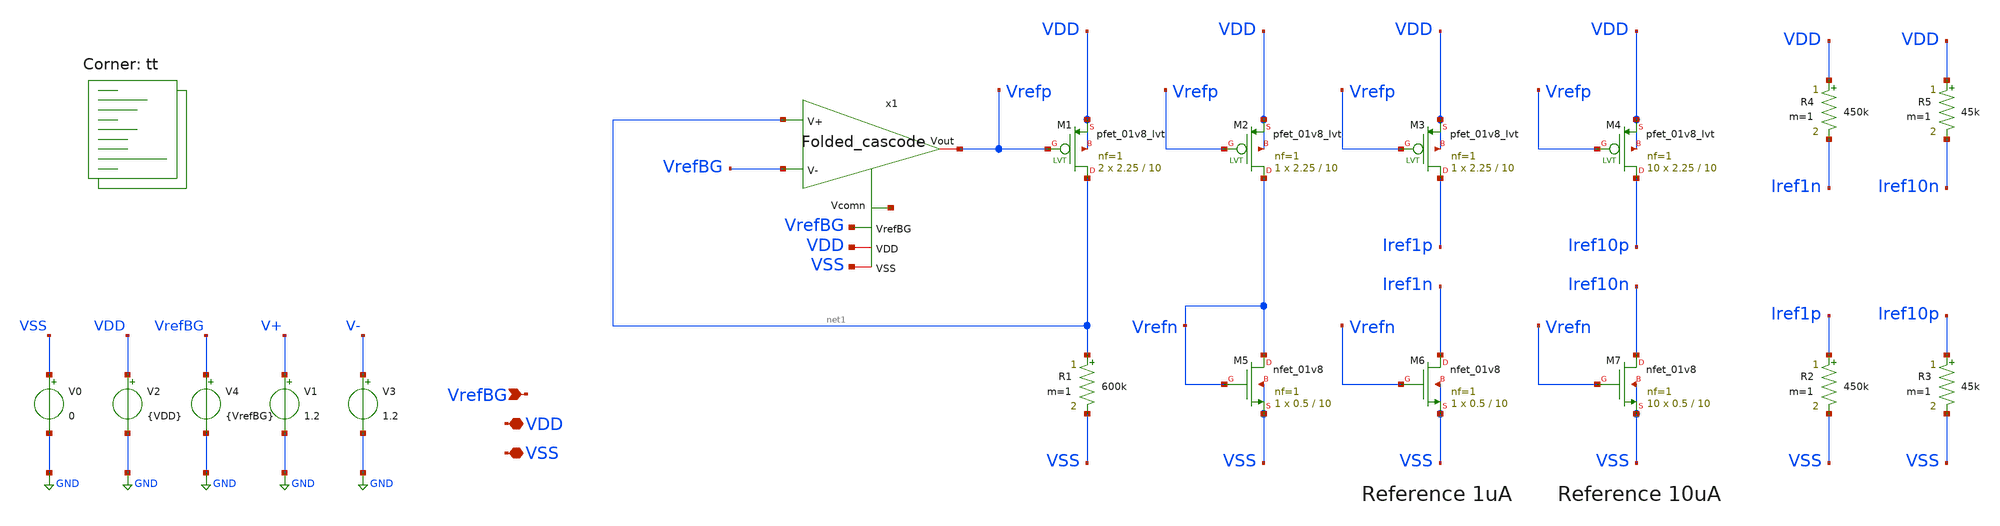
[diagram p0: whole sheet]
** sch_path: openfasoc/generators/curref-gen/sch/Current_reference_generator.sch
**.subckt Current_reference_generator VrefBG VDD VSS
*.ipin VrefBG
*.iopin VDD
*.iopin VSS
x1 Vrefp net1 VrefBG VrefBG VDD VSS net2 Folded_cascode
XM1 net1 Vrefp VDD VDD sky130_fd_pr__pfet_01v8_lvt L=10 W=2.25 nf=1 ad='int((1 + 1)/2) * 2.25 / 1 * 0.29'
+ as='int((1 + 2)/2) * 2.25 / 1 * 0.29' pd='2*int((1 + 1)/2) * (2.25 / 1 + 0.29)' ps='2*int((1 + 2)/2) * (2.25 / 1 + 0.29)'
+ nrd='0.29 / 2.25 ' nrs='0.29 / 2.25 ' sa=0 sb=0 sd=0 mult=2 m=2
R1 net1 VSS 600k m=1
XM2 Vrefn Vrefp VDD VDD sky130_fd_pr__pfet_01v8_lvt L=10 W=2.25 nf=1 ad='int((1 + 1)/2) * 2.25 / 1 * 0.29'
+ as='int((1 + 2)/2) * 2.25 / 1 * 0.29' pd='2*int((1 + 1)/2) * (2.25 / 1 + 0.29)' ps='2*int((1 + 2)/2) * (2.25 / 1 + 0.29)'
+ nrd='0.29 / 2.25 ' nrs='0.29 / 2.25 ' sa=0 sb=0 sd=0 mult=1 m=1
XM5 Vrefn Vrefn VSS VSS sky130_fd_pr__nfet_01v8 L=10 W=0.5 nf=1 ad='int((nf+1)/2) * W/nf * 0.29' as='int((nf+2)/2) * W/nf * 0.29'
+ pd='2*int((nf+1)/2) * (W/nf + 0.29)' ps='2*int((nf+2)/2) * (W/nf + 0.29)' nrd='0.29 / W' nrs='0.29 / W'
+ sa=0 sb=0 sd=0 mult=1 m=1
XM6 Iref1n Vrefn VSS VSS sky130_fd_pr__nfet_01v8 L=10 W=0.5 nf=1 ad='int((nf+1)/2) * W/nf * 0.29' as='int((nf+2)/2) * W/nf * 0.29'
+ pd='2*int((nf+1)/2) * (W/nf + 0.29)' ps='2*int((nf+2)/2) * (W/nf + 0.29)' nrd='0.29 / W' nrs='0.29 / W'
+ sa=0 sb=0 sd=0 mult=1 m=1
XM3 Iref1p Vrefp VDD VDD sky130_fd_pr__pfet_01v8_lvt L=10 W=2.25 nf=1 ad='int((1 + 1)/2) * 2.25 / 1 * 0.29'
+ as='int((1 + 2)/2) * 2.25 / 1 * 0.29' pd='2*int((1 + 1)/2) * (2.25 / 1 + 0.29)' ps='2*int((1 + 2)/2) * (2.25 / 1 + 0.29)'
+ nrd='0.29 / 2.25 ' nrs='0.29 / 2.25 ' sa=0 sb=0 sd=0 mult=1 m=1
XM7 Iref10n Vrefn VSS VSS sky130_fd_pr__nfet_01v8 L=10 W=0.5 nf=1 ad='int((nf+1)/2) * W/nf * 0.29' as='int((nf+2)/2) * W/nf * 0.29'
+ pd='2*int((nf+1)/2) * (W/nf + 0.29)' ps='2*int((nf+2)/2) * (W/nf + 0.29)' nrd='0.29 / W' nrs='0.29 / W'
+ sa=0 sb=0 sd=0 mult=10 m=10
XM4 Iref10p Vrefp VDD VDD sky130_fd_pr__pfet_01v8_lvt L=10 W=2.25 nf=1 ad='int((1 + 1)/2) * 2.25 / 1 * 0.29'
+ as='int((1 + 2)/2) * 2.25 / 1 * 0.29' pd='2*int((1 + 1)/2) * (2.25 / 1 + 0.29)' ps='2*int((1 + 2)/2) * (2.25 / 1 + 0.29)'
+ nrd='0.29 / 2.25 ' nrs='0.29 / 2.25 ' sa=0 sb=0 sd=0 mult=10 m=10
V0 VSS GND 0
V2 VDD GND {VDD}
V4 VrefBG GND {VrefBG}
V1 V+ GND 1.2
V3 V- GND 1.2
R2 Iref1p VSS 450k m=1
R3 Iref10p VSS 45k m=1
R4 VDD Iref1n 450k m=1
R5 VDD Iref10n 45k m=1
**** begin user architecture code
.lib $::SKYWATER_MODELS/sky130.lib.spice tt



.param VDD=1.8
.param VrefBG=1.2
.save

*nfet
  @m.xm5.msky130_fd_pr__nfet_01v8[gm]  v(@m.xm5.msky130_fd_pr__nfet_01v8[vth])
+  @m.xm5.msky130_fd_pr__nfet_01v8[gds]  @m.xm5.msky130_fd_pr__nfet_01v8[id]
  @m.xm6.msky130_fd_pr__nfet_01v8[gm]  v(@m.xm6.msky130_fd_pr__nfet_01v8[vth])
+  @m.xm6.msky130_fd_pr__nfet_01v8[gds]  @m.xm6.msky130_fd_pr__nfet_01v8[id]
  @m.xm7.msky130_fd_pr__nfet_01v8[gm]  v(@m.xm7.msky130_fd_pr__nfet_01v8[vth])
+  @m.xm7.msky130_fd_pr__nfet_01v8[gds]  @m.xm7.msky130_fd_pr__nfet_01v8[id]

*pfet
  @m.xm1.msky130_fd_pr__pfet_01v8_lvt[gm]  v(@m.xm1.msky130_fd_pr__pfet_01v8_lvt[vth])
+  @m.xm1.msky130_fd_pr__pfet_01v8_lvt[gds]  @m.xm1.msky130_fd_pr__pfet_01v8_lvt[id]
  @m.xm2.msky130_fd_pr__pfet_01v8_lvt[gm]  v(@m.xm2.msky130_fd_pr__pfet_01v8_lvt[vth])
+  @m.xm2.msky130_fd_pr__pfet_01v8_lvt[gds]  @m.xm2.msky130_fd_pr__pfet_01v8_lvt[id]
  @m.xm3.msky130_fd_pr__pfet_01v8_lvt[gm]  v(@m.xm3.msky130_fd_pr__pfet_01v8_lvt[vth])
+  @m.xm3.msky130_fd_pr__pfet_01v8_lvt[gds]  @m.xm3.msky130_fd_pr__pfet_01v8_lvt[id]
  @m.xm4.msky130_fd_pr__pfet_01v8_lvt[gm]  v(@m.xm4.msky130_fd_pr__pfet_01v8_lvt[vth])
+  @m.xm4.msky130_fd_pr__pfet_01v8_lvt[gds]  @m.xm4.msky130_fd_pr__pfet_01v8_lvt[id]

.control
  save all
  op
  show
  write Current_reference_generator.raw
.endc



**** end user architecture code
**.ends

* expanding   symbol:  /foss/designs/Folded_cascode/Folded_cascode.sym # of pins=7
** sym_path: openfasoc/generators/curref-gen/sch/Folded_cascode.sym
** sch_path: openfasoc/generators/curref-gen/sch/Folded_cascode.sch
.subckt Folded_cascode Vout V+ V- VrefBG VDD VSS Vcomn
*.ipin V+
*.ipin V-
*.ipin VrefBG
*.iopin VDD
*.iopin VSS
*.iopin Vout
*.iopin Vcomn
XM6 net2 V- net5 net5 sky130_fd_pr__nfet_01v8 L=1 W=1 nf=1 ad='int((nf+1)/2) * W/nf * 0.29' as='int((nf+2)/2) * W/nf * 0.29'
+ pd='2*int((nf+1)/2) * (W/nf + 0.29)' ps='2*int((nf+2)/2) * (W/nf + 0.29)' nrd='0.29 / W' nrs='0.29 / W'
+ sa=0 sb=0 sd=0 mult=20 m=20
XM7 Vout VB2 Vcomn VSS sky130_fd_pr__nfet_01v8 L=3 W=1 nf=1 ad='int((nf+1)/2) * W/nf * 0.29' as='int((nf+2)/2) * W/nf * 0.29'
+ pd='2*int((nf+1)/2) * (W/nf + 0.29)' ps='2*int((nf+2)/2) * (W/nf + 0.29)' nrd='0.29 / W' nrs='0.29 / W'
+ sa=0 sb=0 sd=0 mult=5 m=5
XM8 net4 VB2 net3 VSS sky130_fd_pr__nfet_01v8 L=3 W=1 nf=1 ad='int((nf+1)/2) * W/nf * 0.29' as='int((nf+2)/2) * W/nf * 0.29'
+ pd='2*int((nf+1)/2) * (W/nf + 0.29)' ps='2*int((nf+2)/2) * (W/nf + 0.29)' nrd='0.29 / W' nrs='0.29 / W'
+ sa=0 sb=0 sd=0 mult=5 m=5
XM9 Vcomn VP VSS VSS sky130_fd_pr__nfet_01v8 L=6.5 W=0.5 nf=1 ad='int((nf+1)/2) * W/nf * 0.29' as='int((nf+2)/2) * W/nf * 0.29'
+ pd='2*int((nf+1)/2) * (W/nf + 0.29)' ps='2*int((nf+2)/2) * (W/nf + 0.29)' nrd='0.29 / W' nrs='0.29 / W'
+ sa=0 sb=0 sd=0 mult=5 m=5
XM10 net3 VP VSS VSS sky130_fd_pr__nfet_01v8 L=6.5 W=0.5 nf=1 ad='int((nf+1)/2) * W/nf * 0.29' as='int((nf+2)/2) * W/nf * 0.29'
+ pd='2*int((nf+1)/2) * (W/nf + 0.29)' ps='2*int((nf+2)/2) * (W/nf + 0.29)' nrd='0.29 / W' nrs='0.29 / W'
+ sa=0 sb=0 sd=0 mult=5 m=5
XM11 net5 VP VSS VSS sky130_fd_pr__nfet_01v8 L=6.5 W=0.5 nf=1 ad='int((nf+1)/2) * W/nf * 0.29' as='int((nf+2)/2) * W/nf * 0.29'
+ pd='2*int((nf+1)/2) * (W/nf + 0.29)' ps='2*int((nf+2)/2) * (W/nf + 0.29)' nrd='0.29 / W' nrs='0.29 / W'
+ sa=0 sb=0 sd=0 mult=10 m=10
XM1 net1 V+ net5 net5 sky130_fd_pr__nfet_01v8 L=1 W=1 nf=1 ad='int((nf+1)/2) * W/nf * 0.29' as='int((nf+2)/2) * W/nf * 0.29'
+ pd='2*int((nf+1)/2) * (W/nf + 0.29)' ps='2*int((nf+2)/2) * (W/nf + 0.29)' nrd='0.29 / W' nrs='0.29 / W'
+ sa=0 sb=0 sd=0 mult=20 m=20
XM12 VP VP VSS VSS sky130_fd_pr__nfet_01v8 L=6.5 W=0.5 nf=1 ad='int((nf+1)/2) * W/nf * 0.29' as='int((nf+2)/2) * W/nf * 0.29'
+ pd='2*int((nf+1)/2) * (W/nf + 0.29)' ps='2*int((nf+2)/2) * (W/nf + 0.29)' nrd='0.29 / W' nrs='0.29 / W'
+ sa=0 sb=0 sd=0 mult=1 m=1
XM13 net6 VP VSS VSS sky130_fd_pr__nfet_01v8 L=6.5 W=0.5 nf=1 ad='int((nf+1)/2) * W/nf * 0.29' as='int((nf+2)/2) * W/nf * 0.29'
+ pd='2*int((nf+1)/2) * (W/nf + 0.29)' ps='2*int((nf+2)/2) * (W/nf + 0.29)' nrd='0.29 / W' nrs='0.29 / W'
+ sa=0 sb=0 sd=0 mult=1 m=1
XM17 VB2 VB2 VSS VSS sky130_fd_pr__nfet_01v8 L=18 W=0.42 nf=1 ad='int((nf+1)/2) * W/nf * 0.29' as='int((nf+2)/2) * W/nf * 0.29'
+ pd='2*int((nf+1)/2) * (W/nf + 0.29)' ps='2*int((nf+2)/2) * (W/nf + 0.29)' nrd='0.29 / W' nrs='0.29 / W'
+ sa=0 sb=0 sd=0 mult=1 m=1
XM18 VB2 net6 VDD VDD sky130_fd_pr__pfet_01v8_lvt L=6 W=0.5 nf=1 ad='int((1 + 1)/2) * 0.5 / 1 * 0.29'
+ as='int((1 + 2)/2) * 0.5 / 1 * 0.29' pd='2*int((1 + 1)/2) * (0.5 / 1 + 0.29)' ps='2*int((1 + 2)/2) * (0.5 / 1 + 0.29)'
+ nrd='0.29 / 0.5 ' nrs='0.29 / 0.5 ' sa=0 sb=0 sd=0 mult=4 m=4
XM15 net6 net6 VDD VDD sky130_fd_pr__pfet_01v8_lvt L=6 W=0.5 nf=1 ad='int((1 + 1)/2) * 0.5 / 1 * 0.29'
+ as='int((1 + 2)/2) * 0.5 / 1 * 0.29' pd='2*int((1 + 1)/2) * (0.5 / 1 + 0.29)' ps='2*int((1 + 2)/2) * (0.5 / 1 + 0.29)'
+ nrd='0.29 / 0.5 ' nrs='0.29 / 0.5 ' sa=0 sb=0 sd=0 mult=4 m=4
XM3 net1 net4 VDD VDD sky130_fd_pr__pfet_01v8_lvt L=3 W=1 nf=1 ad='int((1 + 1)/2) * 1 / 1 * 0.29' as='int((1 + 2)/2) * 1 / 1 * 0.29'
+ pd='2*int((1 + 1)/2) * (1 / 1 + 0.29)' ps='2*int((1 + 2)/2) * (1 / 1 + 0.29)' nrd='0.29 / 1 ' nrs='0.29 / 1 '
+ sa=0 sb=0 sd=0 mult=6 m=6
XM2 net2 net4 VDD VDD sky130_fd_pr__pfet_01v8_lvt L=3 W=1 nf=1 ad='int((1 + 1)/2) * 1 / 1 * 0.29' as='int((1 + 2)/2) * 1 / 1 * 0.29'
+ pd='2*int((1 + 1)/2) * (1 / 1 + 0.29)' ps='2*int((1 + 2)/2) * (1 / 1 + 0.29)' nrd='0.29 / 1 ' nrs='0.29 / 1 '
+ sa=0 sb=0 sd=0 mult=6 m=6
XM5 net4 VB1 net1 VDD sky130_fd_pr__pfet_01v8_lvt L=1.5 W=1 nf=1 ad='int((1 + 1)/2) * 1 / 1 * 0.29' as='int((1 + 2)/2) * 1 / 1 * 0.29'
+ pd='2*int((1 + 1)/2) * (1 / 1 + 0.29)' ps='2*int((1 + 2)/2) * (1 / 1 + 0.29)' nrd='0.29 / 1 ' nrs='0.29 / 1 '
+ sa=0 sb=0 sd=0 mult=10 m=10
XM16 Vout VB1 net2 VDD sky130_fd_pr__pfet_01v8_lvt L=1.5 W=1 nf=1 ad='int((1 + 1)/2) * 1 / 1 * 0.29'
+ as='int((1 + 2)/2) * 1 / 1 * 0.29' pd='2*int((1 + 1)/2) * (1 / 1 + 0.29)' ps='2*int((1 + 2)/2) * (1 / 1 + 0.29)'
+ nrd='0.29 / 1 ' nrs='0.29 / 1 ' sa=0 sb=0 sd=0 mult=10 m=10
XM4 VP VB1 VDD VDD sky130_fd_pr__pfet_01v8_lvt L=6 W=0.5 nf=1 ad='int((1 + 1)/2) * 0.5 / 1 * 0.29' as='int((1 + 2)/2) * 0.5 / 1 * 0.29'
+ pd='2*int((1 + 1)/2) * (0.5 / 1 + 0.29)' ps='2*int((1 + 2)/2) * (0.5 / 1 + 0.29)' nrd='0.29 / 0.5 ' nrs='0.29 / 0.5 '
+ sa=0 sb=0 sd=0 mult=1 m=1
XM14 VB1 VB1 VDD VDD sky130_fd_pr__pfet_01v8_lvt L=6 W=0.5 nf=1 ad='int((1 + 1)/2) * 0.5 / 1 * 0.29'
+ as='int((1 + 2)/2) * 0.5 / 1 * 0.29' pd='2*int((1 + 1)/2) * (0.5 / 1 + 0.29)' ps='2*int((1 + 2)/2) * (0.5 / 1 + 0.29)'
+ nrd='0.29 / 0.5 ' nrs='0.29 / 0.5 ' sa=0 sb=0 sd=0 mult=1 m=1
XM19 VB1 VrefBG VSS VSS sky130_fd_pr__nfet_01v8 L=18 W=0.45 nf=1 ad='int((nf+1)/2) * W/nf * 0.29' as='int((nf+2)/2) * W/nf * 0.29'
+ pd='2*int((nf+1)/2) * (W/nf + 0.29)' ps='2*int((nf+2)/2) * (W/nf + 0.29)' nrd='0.29 / W' nrs='0.29 / W'
+ sa=0 sb=0 sd=0 mult=1 m=1
.ends

.GLOBAL GND
.end
